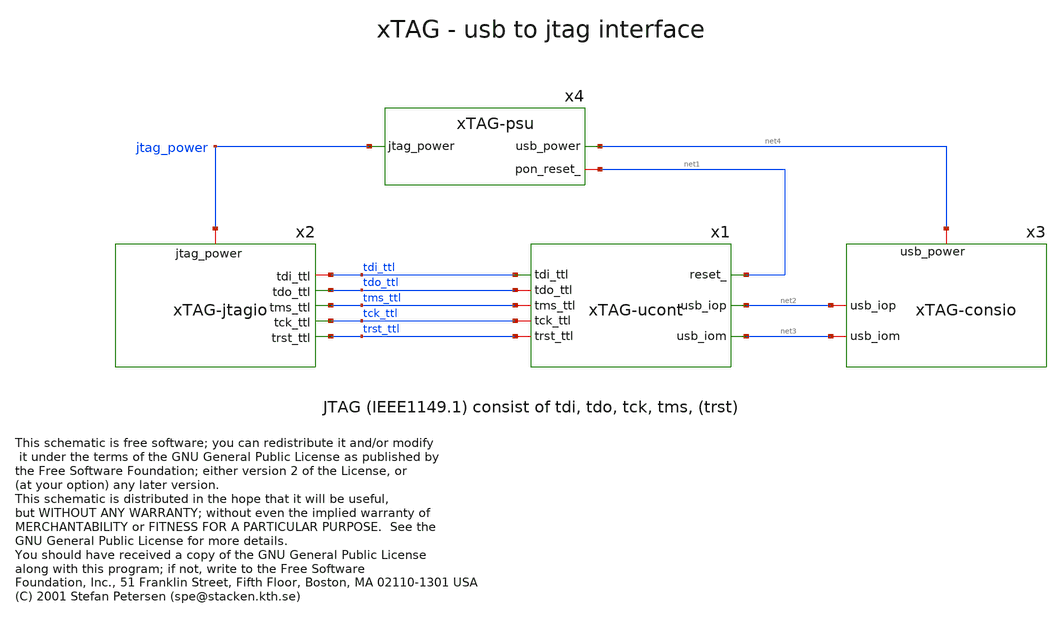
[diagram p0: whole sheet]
** sch_path: xschem_library/xTAG/xTAG.sch
* This schematic is free software; you can redistribute it and/or modify
* it under the terms of the GNU General Public License as published by
* the Free Software Foundation; either version 2 of the License, or
* (at your option) any later version.
* (C) 2001 Stefan Petersen (spe@stacken.kth.se)
**.subckt xTAG
x4 net4 net1 jtag_power xTAG-psu
x2 jtag_power tdi_ttl tdo_ttl tms_ttl tck_ttl trst_ttl xTAG-jtagio
x1 tdi_ttl tdo_ttl tms_ttl tck_ttl trst_ttl net1 net2 net3 xTAG-ucont
x3 net4 net2 net3 xTAG-consio
**.ends
.end
